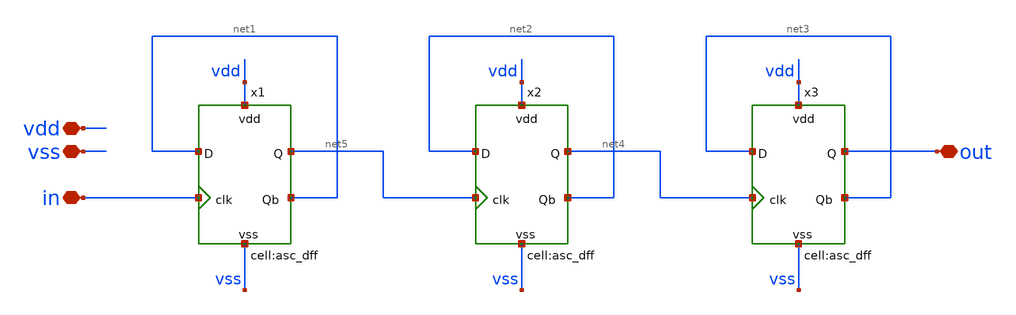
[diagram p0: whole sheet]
** sch_path: designs/libs/xp_core_analog/asc_N_8_divider/asc_N_8_divider.sch
**.subckt asc_N_8_divider vdd vss in out
*.iopin vdd
*.iopin vss
*.iopin in
*.iopin out
x1 in net1 net1 vdd vss net5 asc_dff
x2 net5 net2 net2 vdd vss net4 asc_dff
x3 net4 net3 net3 vdd vss out asc_dff
**.ends
.end
